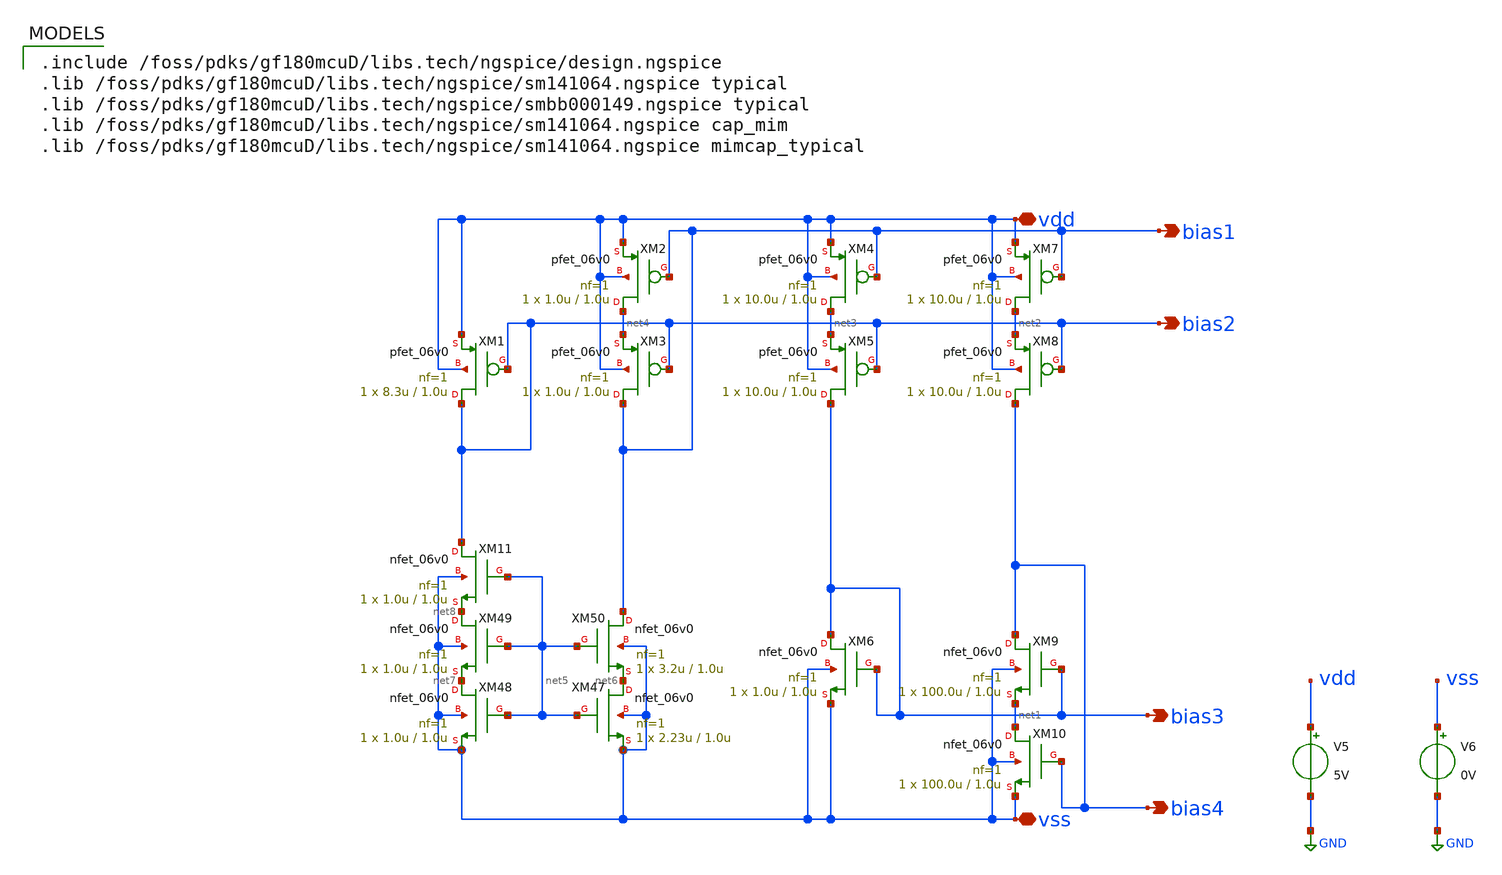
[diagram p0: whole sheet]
** sch_path: activities/opamp2AKAM/simulations_testbench/simulations_testbench/biasTestbench.sch
**.subckt biasTestbench bias1 bias3 bias4 vdd vss bias2
*.opin bias1
*.opin bias3
*.opin bias4
*.iopin vdd
*.iopin vss
*.opin bias2
V5 vdd GND 5V
V6 vss GND 0V
XM4 net3 bias1 vdd vdd pfet_06v0 L=1.0u W=10.0u nf=1 ad='int((nf+1)/2) * W/nf * 0.18u' as='int((nf+2)/2) * W/nf * 0.18u'
+ pd='2*int((nf+1)/2) * (W/nf + 0.18u)' ps='2*int((nf+2)/2) * (W/nf + 0.18u)' nrd='0.18u / W' nrs='0.18u / W'
+ sa=0 sb=0 sd=0 m=1
XM5 bias3 bias2 net3 vdd pfet_06v0 L=1.0u W=10.0u nf=1 ad='int((nf+1)/2) * W/nf * 0.18u' as='int((nf+2)/2) * W/nf * 0.18u'
+ pd='2*int((nf+1)/2) * (W/nf + 0.18u)' ps='2*int((nf+2)/2) * (W/nf + 0.18u)' nrd='0.18u / W' nrs='0.18u / W'
+ sa=0 sb=0 sd=0 m=1
XM6 bias3 bias3 vss vss nfet_06v0 L=1.0u W=1.0u nf=1 ad='int((nf+1)/2) * W/nf * 0.18u' as='int((nf+2)/2) * W/nf * 0.18u'
+ pd='2*int((nf+1)/2) * (W/nf + 0.18u)' ps='2*int((nf+2)/2) * (W/nf + 0.18u)' nrd='0.18u / W' nrs='0.18u / W'
+ sa=0 sb=0 sd=0 m=1
XM7 net2 bias1 vdd vdd pfet_06v0 L=1.0u W=10.0u nf=1 ad='int((nf+1)/2) * W/nf * 0.18u' as='int((nf+2)/2) * W/nf * 0.18u'
+ pd='2*int((nf+1)/2) * (W/nf + 0.18u)' ps='2*int((nf+2)/2) * (W/nf + 0.18u)' nrd='0.18u / W' nrs='0.18u / W'
+ sa=0 sb=0 sd=0 m=1
XM8 bias4 bias2 net2 vdd pfet_06v0 L=1.0u W=10.0u nf=1 ad='int((nf+1)/2) * W/nf * 0.18u' as='int((nf+2)/2) * W/nf * 0.18u'
+ pd='2*int((nf+1)/2) * (W/nf + 0.18u)' ps='2*int((nf+2)/2) * (W/nf + 0.18u)' nrd='0.18u / W' nrs='0.18u / W'
+ sa=0 sb=0 sd=0 m=1
XM9 bias4 bias3 net1 vss nfet_06v0 L=1.0u W=100.0u nf=1 ad='int((nf+1)/2) * W/nf * 0.18u' as='int((nf+2)/2) * W/nf * 0.18u'
+ pd='2*int((nf+1)/2) * (W/nf + 0.18u)' ps='2*int((nf+2)/2) * (W/nf + 0.18u)' nrd='0.18u / W' nrs='0.18u / W'
+ sa=0 sb=0 sd=0 m=1
XM10 net1 bias4 vss vss nfet_06v0 L=1.0u W=100.0u nf=1 ad='int((nf+1)/2) * W/nf * 0.18u' as='int((nf+2)/2) * W/nf * 0.18u'
+ pd='2*int((nf+1)/2) * (W/nf + 0.18u)' ps='2*int((nf+2)/2) * (W/nf + 0.18u)' nrd='0.18u / W' nrs='0.18u / W'
+ sa=0 sb=0 sd=0 m=1
XM1 bias2 bias2 vdd vdd pfet_06v0 L=1.0u W=8.3u nf=1 ad='int((nf+1)/2) * W/nf * 0.18u' as='int((nf+2)/2) * W/nf * 0.18u'
+ pd='2*int((nf+1)/2) * (W/nf + 0.18u)' ps='2*int((nf+2)/2) * (W/nf + 0.18u)' nrd='0.18u / W' nrs='0.18u / W'
+ sa=0 sb=0 sd=0 m=1
XM2 net4 bias1 vdd vdd pfet_06v0 L=1.0u W=1.0u nf=1 ad='int((nf+1)/2) * W/nf * 0.18u' as='int((nf+2)/2) * W/nf * 0.18u'
+ pd='2*int((nf+1)/2) * (W/nf + 0.18u)' ps='2*int((nf+2)/2) * (W/nf + 0.18u)' nrd='0.18u / W' nrs='0.18u / W'
+ sa=0 sb=0 sd=0 m=1
XM3 bias1 bias2 net4 vdd pfet_06v0 L=1.0u W=1.0u nf=1 ad='int((nf+1)/2) * W/nf * 0.18u' as='int((nf+2)/2) * W/nf * 0.18u'
+ pd='2*int((nf+1)/2) * (W/nf + 0.18u)' ps='2*int((nf+2)/2) * (W/nf + 0.18u)' nrd='0.18u / W' nrs='0.18u / W'
+ sa=0 sb=0 sd=0 m=1
XM47 net6 net5 vss vss nfet_06v0 L=1.0u W=2.23u nf=1 ad='int((nf+1)/2) * W/nf * 0.18u' as='int((nf+2)/2) * W/nf * 0.18u'
+ pd='2*int((nf+1)/2) * (W/nf + 0.18u)' ps='2*int((nf+2)/2) * (W/nf + 0.18u)' nrd='0.18u / W' nrs='0.18u / W'
+ sa=0 sb=0 sd=0 m=1
XM48 net7 net5 vss vss nfet_06v0 L=1.0u W=1.0u nf=1 ad='int((nf+1)/2) * W/nf * 0.18u' as='int((nf+2)/2) * W/nf * 0.18u'
+ pd='2*int((nf+1)/2) * (W/nf + 0.18u)' ps='2*int((nf+2)/2) * (W/nf + 0.18u)' nrd='0.18u / W' nrs='0.18u / W'
+ sa=0 sb=0 sd=0 m=1
XM49 net8 net5 net7 vss nfet_06v0 L=1.0u W=1.0u nf=1 ad='int((nf+1)/2) * W/nf * 0.18u' as='int((nf+2)/2) * W/nf * 0.18u'
+ pd='2*int((nf+1)/2) * (W/nf + 0.18u)' ps='2*int((nf+2)/2) * (W/nf + 0.18u)' nrd='0.18u / W' nrs='0.18u / W'
+ sa=0 sb=0 sd=0 m=1
XM50 bias1 net5 net6 vss nfet_06v0 L=1.0u W=3.2u nf=1 ad='int((nf+1)/2) * W/nf * 0.18u' as='int((nf+2)/2) * W/nf * 0.18u'
+ pd='2*int((nf+1)/2) * (W/nf + 0.18u)' ps='2*int((nf+2)/2) * (W/nf + 0.18u)' nrd='0.18u / W' nrs='0.18u / W'
+ sa=0 sb=0 sd=0 m=1
XM11 bias2 net5 net8 vss nfet_06v0 L=1.0u W=1.0u nf=1 ad='int((nf+1)/2) * W/nf * 0.18u' as='int((nf+2)/2) * W/nf * 0.18u'
+ pd='2*int((nf+1)/2) * (W/nf + 0.18u)' ps='2*int((nf+2)/2) * (W/nf + 0.18u)' nrd='0.18u / W' nrs='0.18u / W'
+ sa=0 sb=0 sd=0 m=1
**** begin user architecture code

.include /foss/pdks/gf180mcuD/libs.tech/ngspice/design.ngspice
.lib /foss/pdks/gf180mcuD/libs.tech/ngspice/sm141064.ngspice typical
.lib /foss/pdks/gf180mcuD/libs.tech/ngspice/smbb000149.ngspice typical
.lib /foss/pdks/gf180mcuD/libs.tech/ngspice/sm141064.ngspice cap_mim
.lib /foss/pdks/gf180mcuD/libs.tech/ngspice/sm141064.ngspice mimcap_typical




.control
  op
  let b1 = v(bias1)
  let b2 = v(bias2)
  let b3 = v(bias3)
  let b4 = v(bias4)
  echo "$&b1 $&b2 $&b3 $&b4" >>
+ /foss/designs/sscs-2026-zotnetic/activities/opamp2AKAM/simulations_testbench/simulation_results/biasTestBench.txt
.endc

**** end user architecture code
**.ends
.GLOBAL GND
.end
